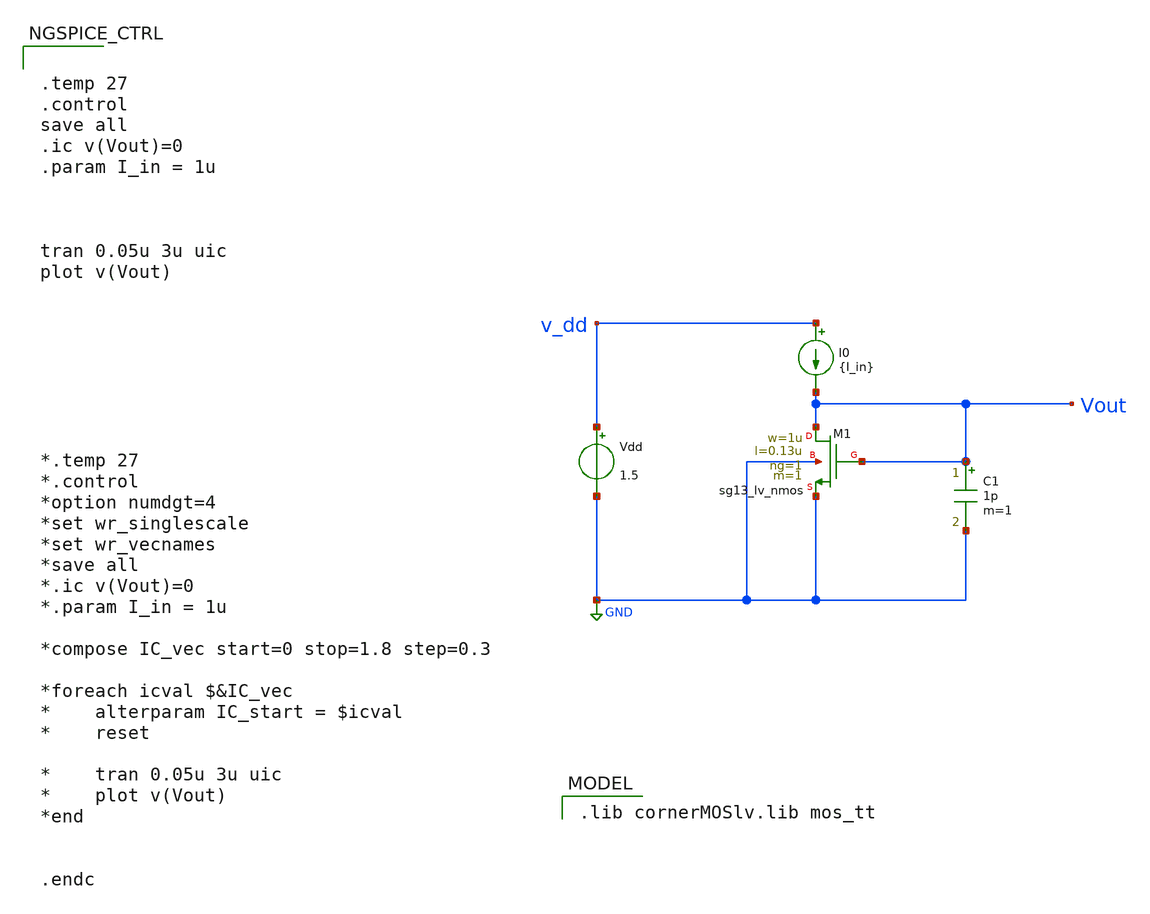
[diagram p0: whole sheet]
** sch_path: assignment_1.sch
**.subckt assignment_1
I0 v_dd Vout {I_in}
XM1 Vout Vout GND GND sg13_lv_nmos w=1u l=0.13u ng=1 m=1 mm_ok=1
C1 Vout GND 1p m=1
Vdd v_dd GND 1.5
**** begin user architecture code


.temp 27
.control
save all
.ic v(Vout)=0
.param I_in = 1u



tran 0.05u 3u uic
plot v(Vout)








*.temp 27
*.control
*option numdgt=4
*set wr_singlescale
*set wr_vecnames
*save all
*.ic v(Vout)=0
*.param I_in = 1u

*compose IC_vec start=0 stop=1.8 step=0.3

*foreach icval $&IC_vec
*    alterparam IC_start = $icval
*    reset

*    tran 0.05u 3u uic
*    plot v(Vout)
*end


.endc


 .lib cornerMOSlv.lib mos_tt

**** end user architecture code
**.ends
.GLOBAL GND
.end
